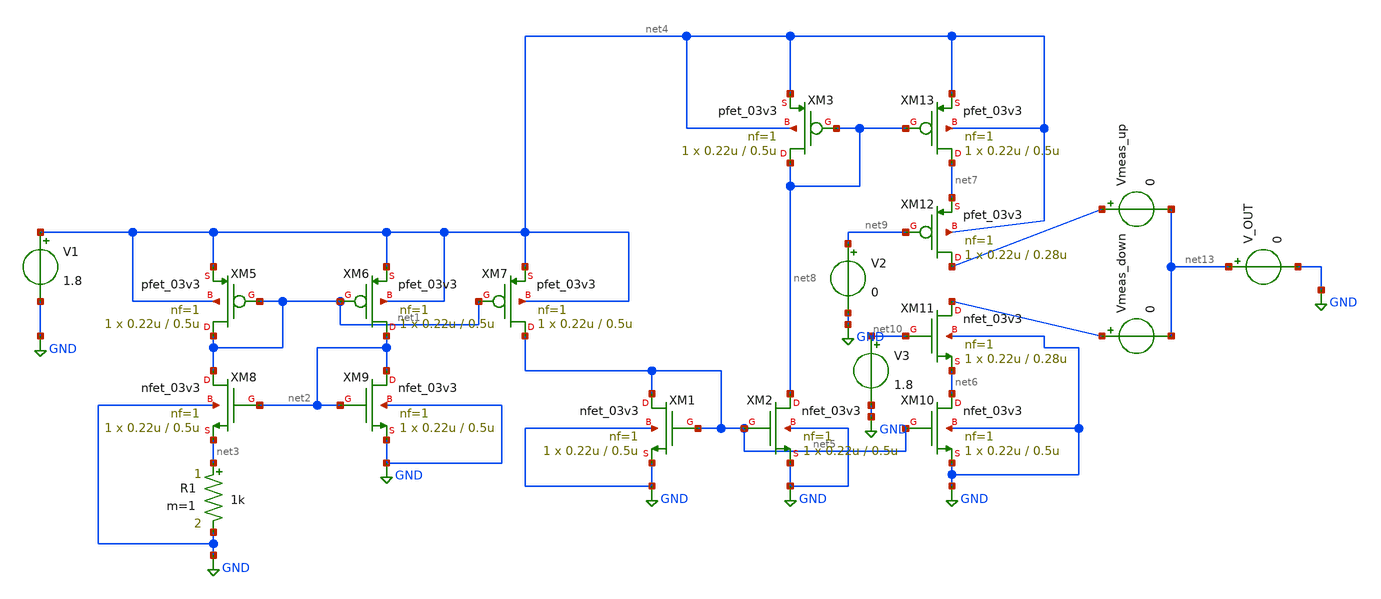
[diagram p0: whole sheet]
** sch_path: src/ChargePump/cp_simple.sch
* Copyright 2022 GlobalFoundries PDK Authors
* Licensed under the Apache License, Version 2.0 (the "License");
* you may not use this file except in compliance with the License.
* You may obtain a copy of the License at
* https://www.apache.org/licenses/LICENSE-2.0
* Unless required by applicable law or agreed to in writing, software
* distributed under the License is distributed on an "AS IS" BASIS,
* WITHOUT WARRANTIES OR CONDITIONS OF ANY KIND, either express or implied.
* See the License for the specific language governing permissions and
* limitations under the License.
**.subckt cp_simple
XM1 net5 net5 GND GND nfet_03v3 L=0.5u W=0.22u nf=1 ad='int((nf+1)/2) * W/nf * 0.18u' as='int((nf+2)/2) * W/nf * 0.18u'
+ pd='2*int((nf+1)/2) * (W/nf + 0.18u)' ps='2*int((nf+2)/2) * (W/nf + 0.18u)' nrd='0.18u / W' nrs='0.18u / W'
+ sa=0 sb=0 sd=0 m=1
XM2 net8 net5 GND GND nfet_03v3 L=0.5u W=0.22u nf=1 ad='int((nf+1)/2) * W/nf * 0.18u' as='int((nf+2)/2) * W/nf * 0.18u'
+ pd='2*int((nf+1)/2) * (W/nf + 0.18u)' ps='2*int((nf+2)/2) * (W/nf + 0.18u)' nrd='0.18u / W' nrs='0.18u / W'
+ sa=0 sb=0 sd=0 m=1
XM3 net8 net8 net4 net4 pfet_03v3 L=0.5u W=0.22u nf=1 ad='int((nf+1)/2) * W/nf * 0.18u' as='int((nf+2)/2) * W/nf * 0.18u'
+ pd='2*int((nf+1)/2) * (W/nf + 0.18u)' ps='2*int((nf+2)/2) * (W/nf + 0.18u)' nrd='0.18u / W' nrs='0.18u / W'
+ sa=0 sb=0 sd=0 m=1
V1 net4 GND 1.8
XM5 net1 net1 net4 net4 pfet_03v3 L=0.5u W=0.22u nf=1 ad='int((nf+1)/2) * W/nf * 0.18u' as='int((nf+2)/2) * W/nf * 0.18u'
+ pd='2*int((nf+1)/2) * (W/nf + 0.18u)' ps='2*int((nf+2)/2) * (W/nf + 0.18u)' nrd='0.18u / W' nrs='0.18u / W'
+ sa=0 sb=0 sd=0 m=1
XM6 net2 net1 net4 net4 pfet_03v3 L=0.5u W=0.22u nf=1 ad='int((nf+1)/2) * W/nf * 0.18u' as='int((nf+2)/2) * W/nf * 0.18u'
+ pd='2*int((nf+1)/2) * (W/nf + 0.18u)' ps='2*int((nf+2)/2) * (W/nf + 0.18u)' nrd='0.18u / W' nrs='0.18u / W'
+ sa=0 sb=0 sd=0 m=1
XM7 net5 net1 net4 net4 pfet_03v3 L=0.5u W=0.22u nf=1 ad='int((nf+1)/2) * W/nf * 0.18u' as='int((nf+2)/2) * W/nf * 0.18u'
+ pd='2*int((nf+1)/2) * (W/nf + 0.18u)' ps='2*int((nf+2)/2) * (W/nf + 0.18u)' nrd='0.18u / W' nrs='0.18u / W'
+ sa=0 sb=0 sd=0 m=1
XM8 net1 net2 net3 GND nfet_03v3 L=0.5u W=0.22u nf=1 ad='int((nf+1)/2) * W/nf * 0.18u' as='int((nf+2)/2) * W/nf * 0.18u'
+ pd='2*int((nf+1)/2) * (W/nf + 0.18u)' ps='2*int((nf+2)/2) * (W/nf + 0.18u)' nrd='0.18u / W' nrs='0.18u / W'
+ sa=0 sb=0 sd=0 m=1
XM9 net2 net2 GND GND nfet_03v3 L=0.5u W=0.22u nf=1 ad='int((nf+1)/2) * W/nf * 0.18u' as='int((nf+2)/2) * W/nf * 0.18u'
+ pd='2*int((nf+1)/2) * (W/nf + 0.18u)' ps='2*int((nf+2)/2) * (W/nf + 0.18u)' nrd='0.18u / W' nrs='0.18u / W'
+ sa=0 sb=0 sd=0 m=1
R1 net3 GND 1k m=1
XM10 net6 net5 GND GND nfet_03v3 L=0.5u W=0.22u nf=1 ad='int((nf+1)/2) * W/nf * 0.18u' as='int((nf+2)/2) * W/nf * 0.18u'
+ pd='2*int((nf+1)/2) * (W/nf + 0.18u)' ps='2*int((nf+2)/2) * (W/nf + 0.18u)' nrd='0.18u / W' nrs='0.18u / W'
+ sa=0 sb=0 sd=0 m=1
XM11 net12 net10 net6 GND nfet_03v3 L=0.28u W=0.22u nf=1 ad='int((nf+1)/2) * W/nf * 0.18u' as='int((nf+2)/2) * W/nf * 0.18u'
+ pd='2*int((nf+1)/2) * (W/nf + 0.18u)' ps='2*int((nf+2)/2) * (W/nf + 0.18u)' nrd='0.18u / W' nrs='0.18u / W'
+ sa=0 sb=0 sd=0 m=1
XM12 net11 net9 net7 net4 pfet_03v3 L=0.28u W=0.22u nf=1 ad='int((nf+1)/2) * W/nf * 0.18u' as='int((nf+2)/2) * W/nf * 0.18u'
+ pd='2*int((nf+1)/2) * (W/nf + 0.18u)' ps='2*int((nf+2)/2) * (W/nf + 0.18u)' nrd='0.18u / W' nrs='0.18u / W'
+ sa=0 sb=0 sd=0 m=1
XM13 net7 net8 net4 net4 pfet_03v3 L=0.5u W=0.22u nf=1 ad='int((nf+1)/2) * W/nf * 0.18u' as='int((nf+2)/2) * W/nf * 0.18u'
+ pd='2*int((nf+1)/2) * (W/nf + 0.18u)' ps='2*int((nf+2)/2) * (W/nf + 0.18u)' nrd='0.18u / W' nrs='0.18u / W'
+ sa=0 sb=0 sd=0 m=1
V2 net9 GND 0
V3 net10 GND 1.8
Vmeas_up net11 net13 0
Vmeas_down net12 net13 0
V_OUT net13 GND 0
**** begin user architecture code

* Include global parameters
.include /foss/pdks/gf180mcuD/libs.tech/ngspice/design.ngspice

*Include the GF180MCU models
.lib /foss/pdks/gf180mcuD/libs.tech/ngspice/sm141064.ngspice typical

.control
* Save the currents flowing through the dummy voltage sources
save I(Vmeas_up) I(Vmeas_down)

* Sweep the output voltage (V_OUT) from 0V to 1.8V in 1mV steps
dc V_OUT 0 1.8 0.001

* Plot the absolute values of the currents
plot abs(I(Vmeas_up)) abs(I(Vmeas_down)) xlabel 'Output Voltage (V)' ylabel 'Charge/Discharge Current (A)'
+ title 'Simple Charge Pump Current Mismatch'
.endc

**** end user architecture code
**.ends
.GLOBAL GND
.end
